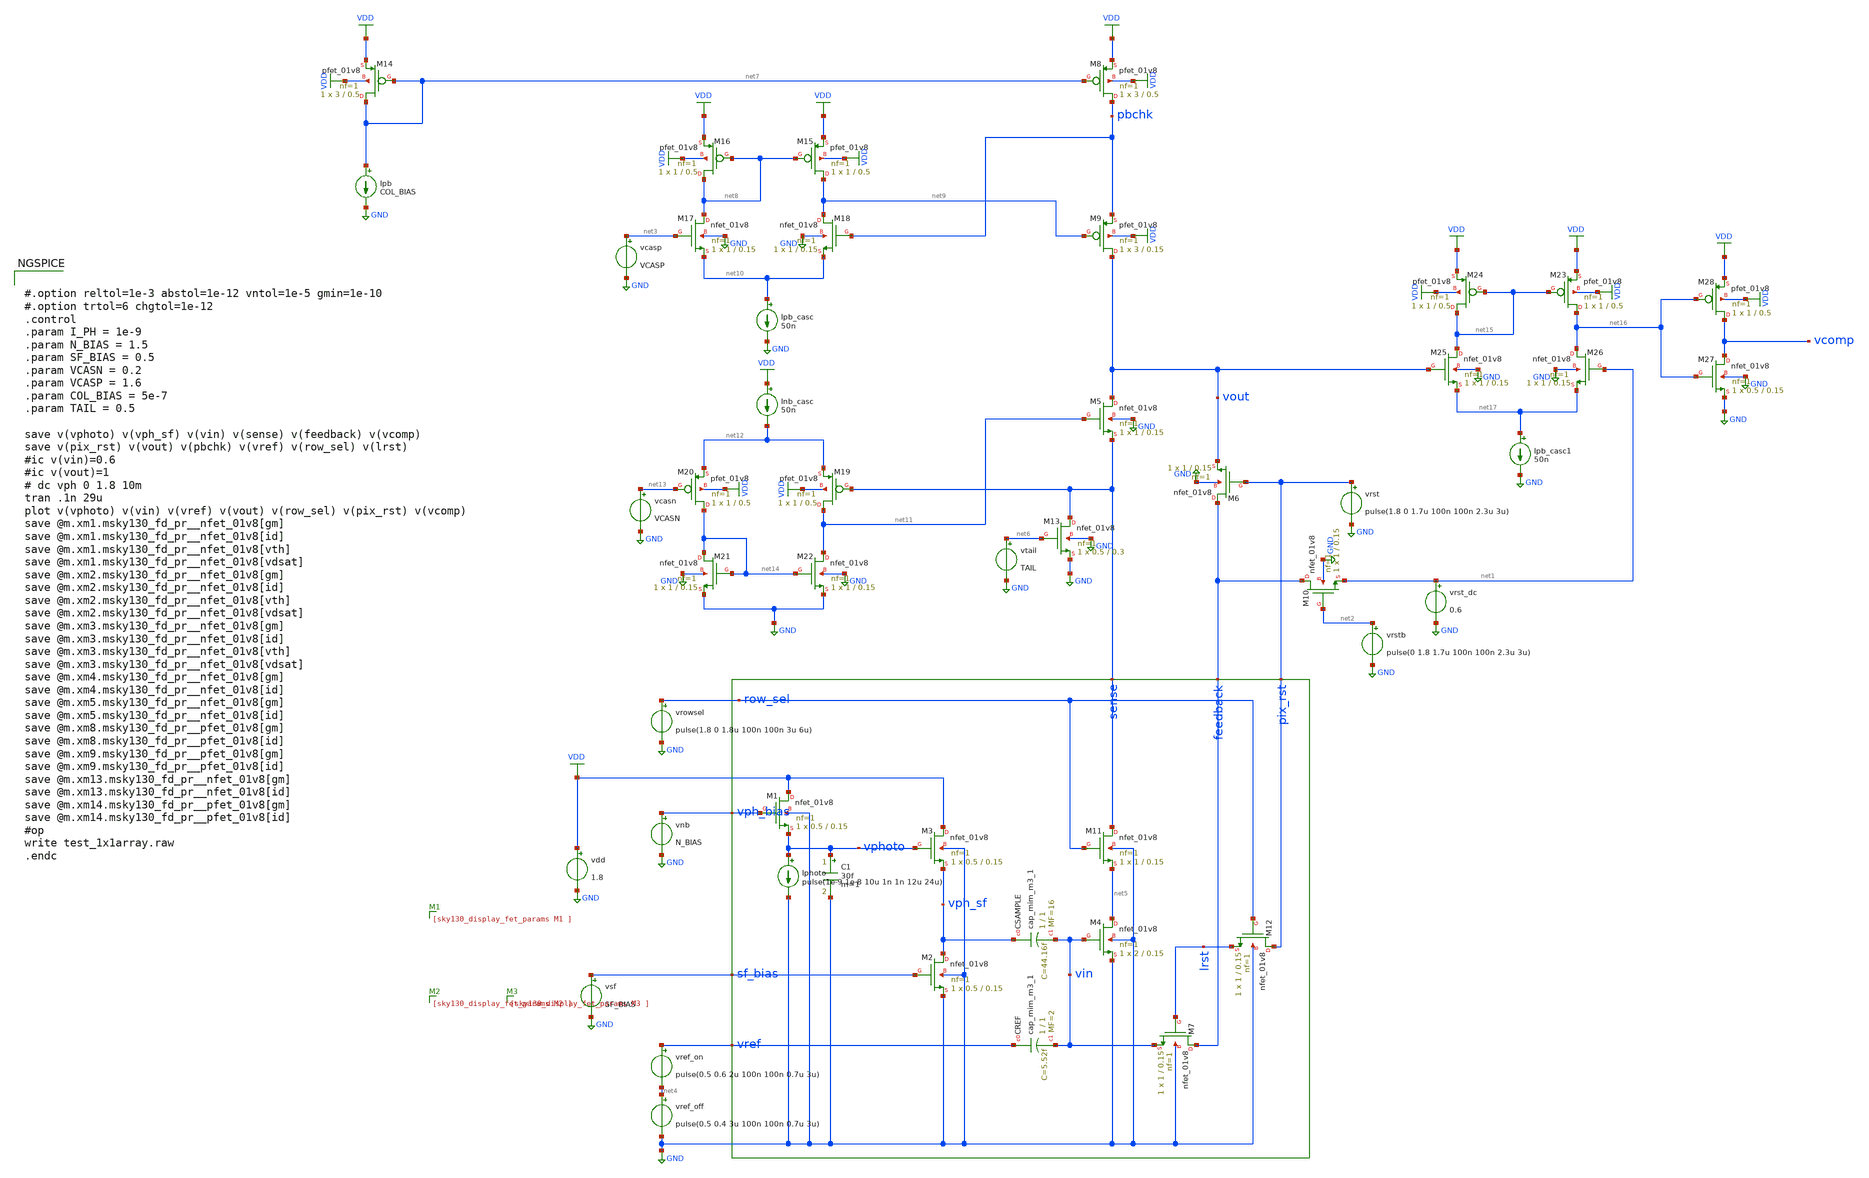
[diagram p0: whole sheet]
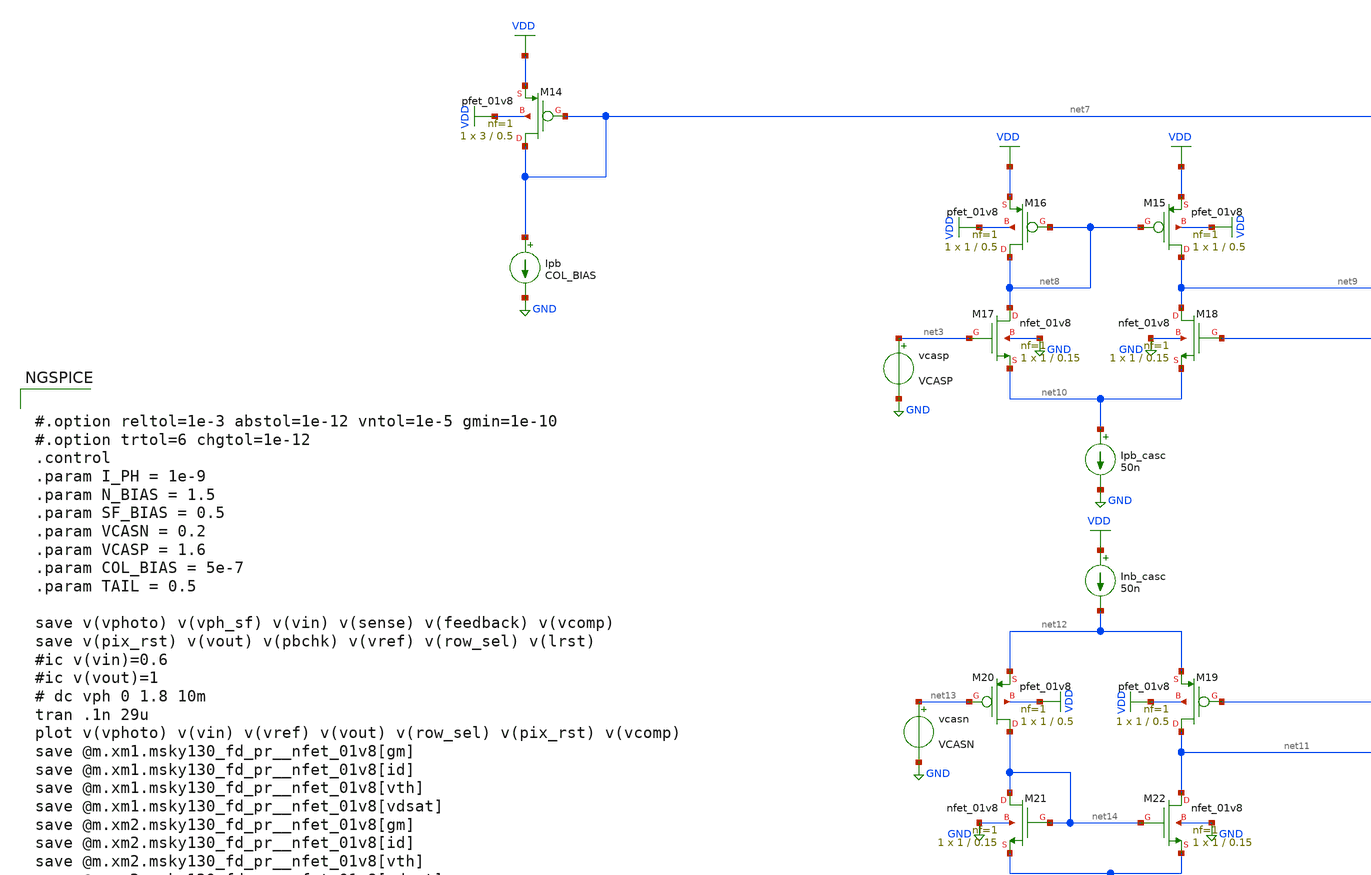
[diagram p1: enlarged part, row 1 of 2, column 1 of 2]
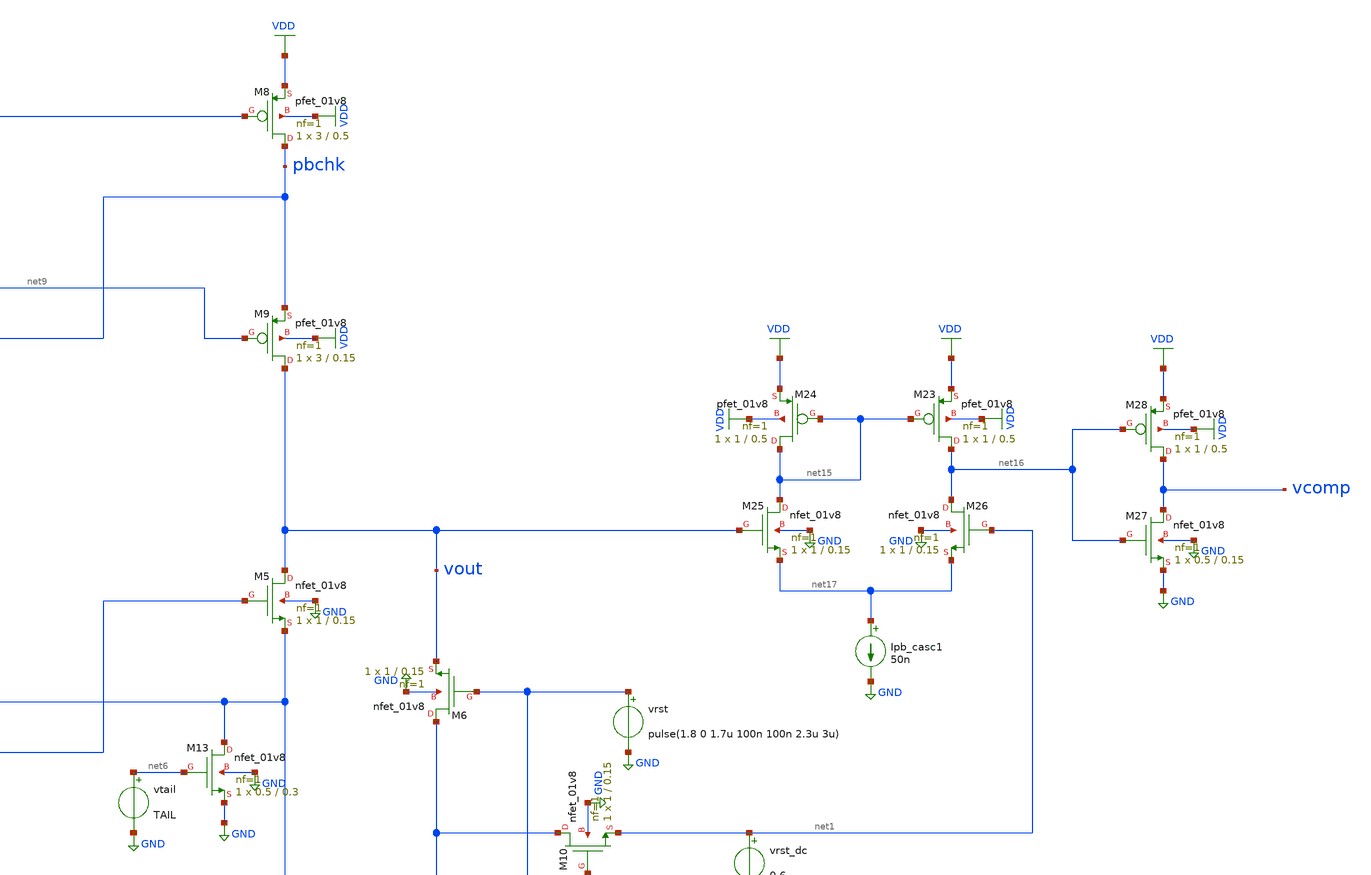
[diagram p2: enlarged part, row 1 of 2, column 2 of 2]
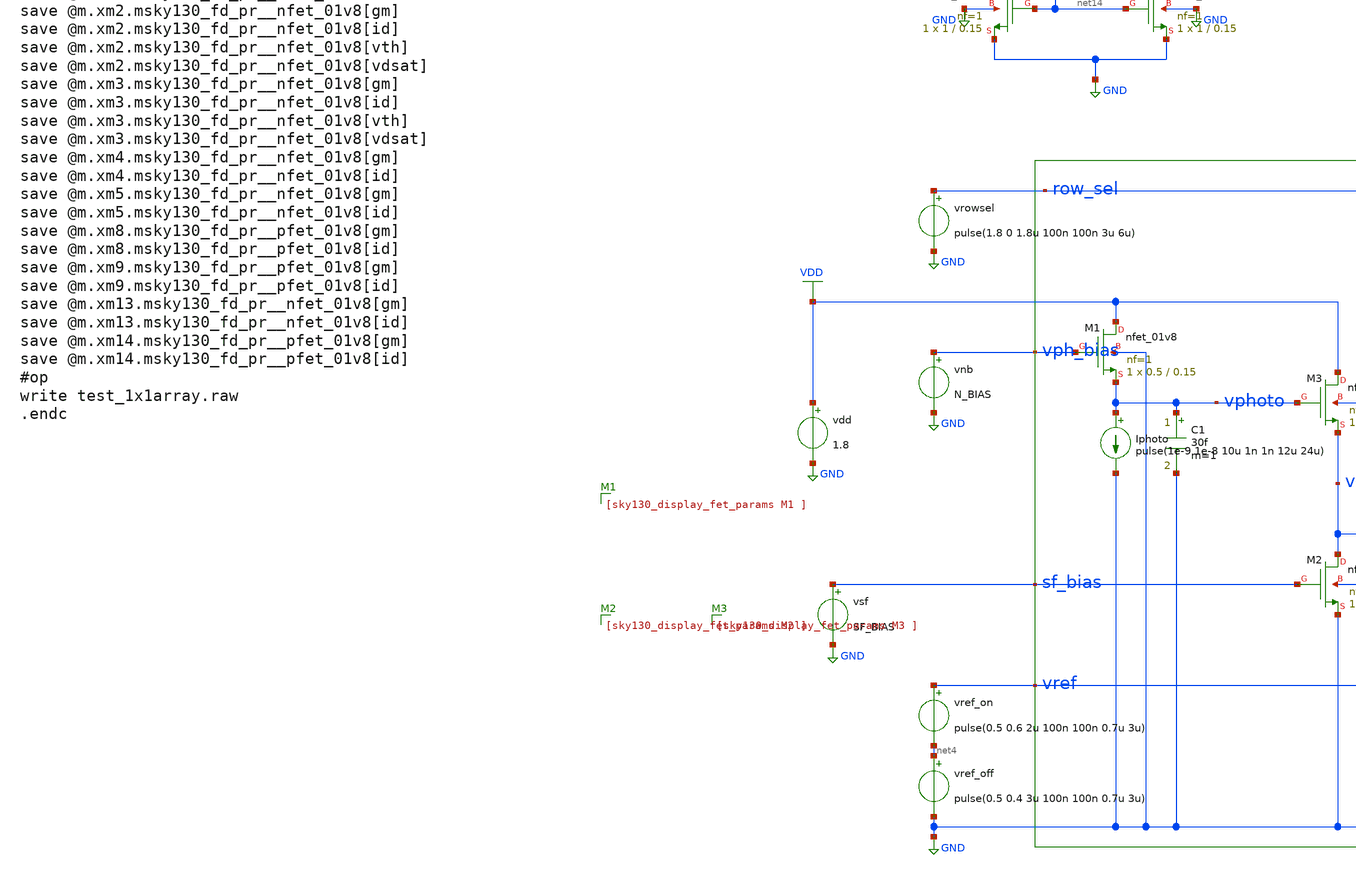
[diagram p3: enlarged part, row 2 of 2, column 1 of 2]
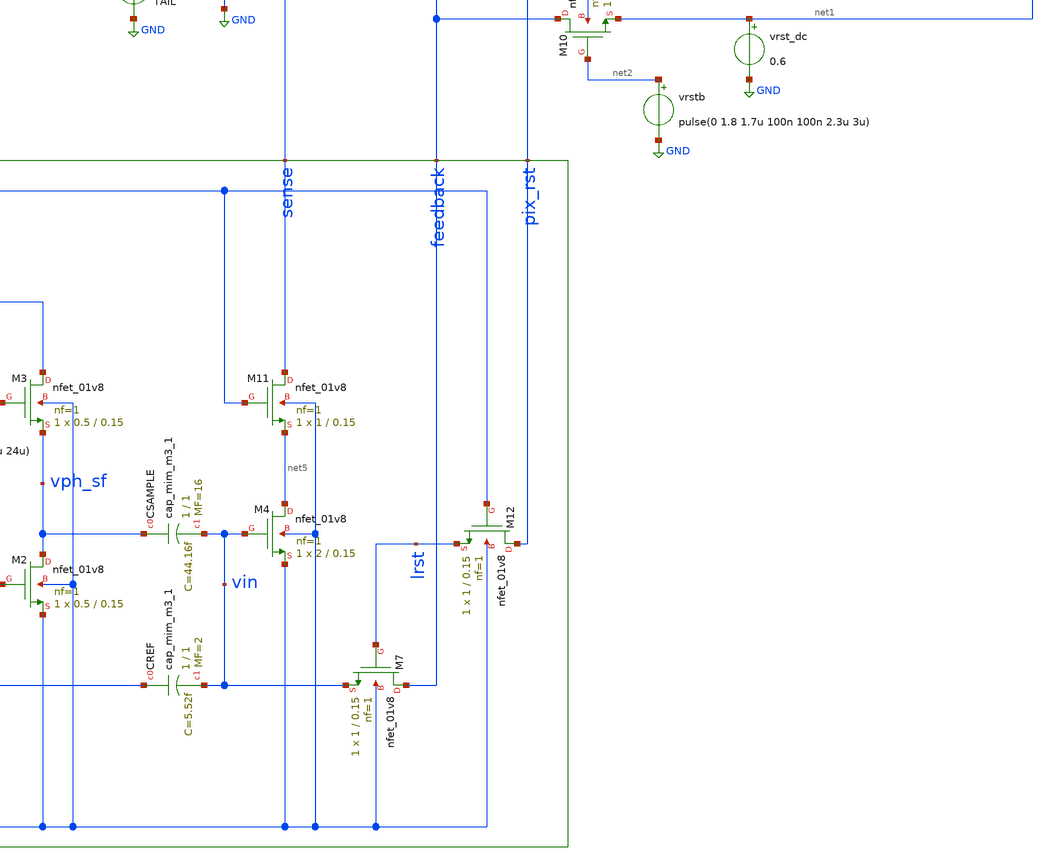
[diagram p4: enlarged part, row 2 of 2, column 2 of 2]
** sch_path: analog/xschem/test_1x1array_v1_good.sch
**.subckt test_1x1array_v1_good
vdd VDD GND 1.8
.save i(vdd)
XCSAMPLE vph_sf vin sky130_fd_pr__cap_mim_m3_1 W=1 L=1 MF=16 m=16
XCREF vref vin sky130_fd_pr__cap_mim_m3_1 W=1 L=1 MF=2 m=2
C1 vphoto GND 30f m=1
XM1 VDD vph_bias vphoto GND sky130_fd_pr__nfet_01v8 L=0.15 W=0.5 nf=1 ad='int((1 + 1)/2) * 0.5 / 1 * 0.29'
+ as='int((1 + 2)/2) * 0.5 / 1 * 0.29' pd='2*int((1 + 1)/2) * (0.5 / 1 + 0.29)' ps='2*int((1 + 2)/2) * (0.5 / 1 + 0.29)'
+ nrd='0.29 / 0.5 ' nrs='0.29 / 0.5 ' sa=0 sb=0 sd=0 mult=1 m=1
vnb vph_bias GND N_BIAS
vsf sf_bias GND SF_BIAS
vref_on vref net4 pulse(0.5 0.6 2u 100n 100n 0.7u 3u)
Iphoto vphoto GND pulse(1e-9 1e-8 10u 1n 1n 12u 24u)
XM4 net5 vin GND GND sky130_fd_pr__nfet_01v8 L=0.15 W=2 nf=1 ad='int((1 + 1)/2) * 2 / 1 * 0.29' as='int((1 + 2)/2) * 2 / 1 * 0.29'
+ pd='2*int((1 + 1)/2) * (2 / 1 + 0.29)' ps='2*int((1 + 2)/2) * (2 / 1 + 0.29)' nrd='0.29 / 2 ' nrs='0.29 / 2 '
+ sa=0 sb=0 sd=0 mult=1 m=1
XM5 vout net11 sense GND sky130_fd_pr__nfet_01v8 L=0.15 W=1 nf=1 ad='int((1 + 1)/2) * 1 / 1 * 0.29' as='int((1 + 2)/2) * 1 / 1 * 0.29'
+ pd='2*int((1 + 1)/2) * (1 / 1 + 0.29)' ps='2*int((1 + 2)/2) * (1 / 1 + 0.29)' nrd='0.29 / 1 ' nrs='0.29 / 1 '
+ sa=0 sb=0 sd=0 mult=1 m=1
vcasn net13 GND VCASN
XM6 feedback pix_rst vout GND sky130_fd_pr__nfet_01v8 L=0.15 W=1 nf=1 ad='int((1 + 1)/2) * 1 / 1 * 0.29'
+ as='int((1 + 2)/2) * 1 / 1 * 0.29' pd='2*int((1 + 1)/2) * (1 / 1 + 0.29)' ps='2*int((1 + 2)/2) * (1 / 1 + 0.29)'
+ nrd='0.29 / 1 ' nrs='0.29 / 1 ' sa=0 sb=0 sd=0 mult=1 m=1
XM7 feedback lrst vin GND sky130_fd_pr__nfet_01v8 L=0.15 W=1 nf=1 ad='int((1 + 1)/2) * 1 / 1 * 0.29'
+ as='int((1 + 2)/2) * 1 / 1 * 0.29' pd='2*int((1 + 1)/2) * (1 / 1 + 0.29)' ps='2*int((1 + 2)/2) * (1 / 1 + 0.29)'
+ nrd='0.29 / 1 ' nrs='0.29 / 1 ' sa=0 sb=0 sd=0 mult=1 m=1
vrst pix_rst GND pulse(1.8 0 1.7u 100n 100n 2.3u 3u)
Ipb net7 GND COL_BIAS
XM8 pbchk net7 VDD VDD sky130_fd_pr__pfet_01v8 L=0.5 W=3 nf=1 ad='int((1 + 1)/2) * 3 / 1 * 0.29' as='int((1 + 2)/2) * 3 / 1 * 0.29'
+ pd='2*int((1 + 1)/2) * (3 / 1 + 0.29)' ps='2*int((1 + 2)/2) * (3 / 1 + 0.29)' nrd='0.29 / 3 ' nrs='0.29 / 3 '
+ sa=0 sb=0 sd=0 mult=1 m=1
XM9 vout net9 pbchk VDD sky130_fd_pr__pfet_01v8 L=0.15 W=3 nf=1 ad='int((1 + 1)/2) * 3 / 1 * 0.29' as='int((1 + 2)/2) * 3 / 1 * 0.29'
+ pd='2*int((1 + 1)/2) * (3 / 1 + 0.29)' ps='2*int((1 + 2)/2) * (3 / 1 + 0.29)' nrd='0.29 / 3 ' nrs='0.29 / 3 '
+ sa=0 sb=0 sd=0 mult=1 m=1
vcasp net3 GND VCASP
XM10 feedback net2 net1 GND sky130_fd_pr__nfet_01v8 L=0.15 W=1 nf=1 ad='int((1 + 1)/2) * 1 / 1 * 0.29'
+ as='int((1 + 2)/2) * 1 / 1 * 0.29' pd='2*int((1 + 1)/2) * (1 / 1 + 0.29)' ps='2*int((1 + 2)/2) * (1 / 1 + 0.29)'
+ nrd='0.29 / 1 ' nrs='0.29 / 1 ' sa=0 sb=0 sd=0 mult=1 m=1
vrstb net2 GND pulse(0 1.8 1.7u 100n 100n 2.3u 3u)
vrst_dc net1 GND 0.6
vref_off net4 GND pulse(0.5 0.4 3u 100n 100n 0.7u 3u)
XM2 vph_sf sf_bias GND GND sky130_fd_pr__nfet_01v8 L=0.15 W=0.5 nf=1 ad='int((1 + 1)/2) * 0.5 / 1 * 0.29'
+ as='int((1 + 2)/2) * 0.5 / 1 * 0.29' pd='2*int((1 + 1)/2) * (0.5 / 1 + 0.29)' ps='2*int((1 + 2)/2) * (0.5 / 1 + 0.29)'
+ nrd='0.29 / 0.5 ' nrs='0.29 / 0.5 ' sa=0 sb=0 sd=0 mult=1 m=1
XM3 VDD vphoto vph_sf GND sky130_fd_pr__nfet_01v8 L=0.15 W=0.5 nf=1 ad='int((1 + 1)/2) * 0.5 / 1 * 0.29'
+ as='int((1 + 2)/2) * 0.5 / 1 * 0.29' pd='2*int((1 + 1)/2) * (0.5 / 1 + 0.29)' ps='2*int((1 + 2)/2) * (0.5 / 1 + 0.29)'
+ nrd='0.29 / 0.5 ' nrs='0.29 / 0.5 ' sa=0 sb=0 sd=0 mult=1 m=1
XM11 sense row_sel net5 GND sky130_fd_pr__nfet_01v8 L=0.15 W=1 nf=1 ad='int((1 + 1)/2) * 1 / 1 * 0.29'
+ as='int((1 + 2)/2) * 1 / 1 * 0.29' pd='2*int((1 + 1)/2) * (1 / 1 + 0.29)' ps='2*int((1 + 2)/2) * (1 / 1 + 0.29)'
+ nrd='0.29 / 1 ' nrs='0.29 / 1 ' sa=0 sb=0 sd=0 mult=1 m=1
XM12 pix_rst row_sel lrst GND sky130_fd_pr__nfet_01v8 L=0.15 W=1 nf=1 ad='int((1 + 1)/2) * 1 / 1 * 0.29'
+ as='int((1 + 2)/2) * 1 / 1 * 0.29' pd='2*int((1 + 1)/2) * (1 / 1 + 0.29)' ps='2*int((1 + 2)/2) * (1 / 1 + 0.29)'
+ nrd='0.29 / 1 ' nrs='0.29 / 1 ' sa=0 sb=0 sd=0 mult=1 m=1
vrowsel row_sel GND pulse(1.8 0 1.8u 100n 100n 3u 6u)
vtail net6 GND TAIL
XM13 sense net6 GND GND sky130_fd_pr__nfet_01v8 L=0.3 W=0.5 nf=1 ad='int((1 + 1)/2) * 0.5 / 1 * 0.29'
+ as='int((1 + 2)/2) * 0.5 / 1 * 0.29' pd='2*int((1 + 1)/2) * (0.5 / 1 + 0.29)' ps='2*int((1 + 2)/2) * (0.5 / 1 + 0.29)'
+ nrd='0.29 / 0.5 ' nrs='0.29 / 0.5 ' sa=0 sb=0 sd=0 mult=1 m=1
XM14 net7 net7 VDD VDD sky130_fd_pr__pfet_01v8 L=0.5 W=3 nf=1 ad='int((1 + 1)/2) * 3 / 1 * 0.29' as='int((1 + 2)/2) * 3 / 1 * 0.29'
+ pd='2*int((1 + 1)/2) * (3 / 1 + 0.29)' ps='2*int((1 + 2)/2) * (3 / 1 + 0.29)' nrd='0.29 / 3 ' nrs='0.29 / 3 '
+ sa=0 sb=0 sd=0 mult=1 m=1
XM15 net9 net8 VDD VDD sky130_fd_pr__pfet_01v8 L=0.5 W=1 nf=1 ad='int((1 + 1)/2) * 1 / 1 * 0.29' as='int((1 + 2)/2) * 1 / 1 * 0.29'
+ pd='2*int((1 + 1)/2) * (1 / 1 + 0.29)' ps='2*int((1 + 2)/2) * (1 / 1 + 0.29)' nrd='0.29 / 1 ' nrs='0.29 / 1 '
+ sa=0 sb=0 sd=0 mult=1 m=1
XM16 net8 net8 VDD VDD sky130_fd_pr__pfet_01v8 L=0.5 W=1 nf=1 ad='int((1 + 1)/2) * 1 / 1 * 0.29' as='int((1 + 2)/2) * 1 / 1 * 0.29'
+ pd='2*int((1 + 1)/2) * (1 / 1 + 0.29)' ps='2*int((1 + 2)/2) * (1 / 1 + 0.29)' nrd='0.29 / 1 ' nrs='0.29 / 1 '
+ sa=0 sb=0 sd=0 mult=1 m=1
XM17 net8 net3 net10 GND sky130_fd_pr__nfet_01v8 L=0.15 W=1 nf=1 ad='int((1 + 1)/2) * 1 / 1 * 0.29' as='int((1 + 2)/2) * 1 / 1 * 0.29'
+ pd='2*int((1 + 1)/2) * (1 / 1 + 0.29)' ps='2*int((1 + 2)/2) * (1 / 1 + 0.29)' nrd='0.29 / 1 ' nrs='0.29 / 1 '
+ sa=0 sb=0 sd=0 mult=1 m=1
XM18 net9 pbchk net10 GND sky130_fd_pr__nfet_01v8 L=0.15 W=1 nf=1 ad='int((1 + 1)/2) * 1 / 1 * 0.29'
+ as='int((1 + 2)/2) * 1 / 1 * 0.29' pd='2*int((1 + 1)/2) * (1 / 1 + 0.29)' ps='2*int((1 + 2)/2) * (1 / 1 + 0.29)'
+ nrd='0.29 / 1 ' nrs='0.29 / 1 ' sa=0 sb=0 sd=0 mult=1 m=1
Ipb_casc net10 GND 50n
XM19 net11 sense net12 VDD sky130_fd_pr__pfet_01v8 L=0.5 W=1 nf=1 ad='int((1 + 1)/2) * 1 / 1 * 0.29'
+ as='int((1 + 2)/2) * 1 / 1 * 0.29' pd='2*int((1 + 1)/2) * (1 / 1 + 0.29)' ps='2*int((1 + 2)/2) * (1 / 1 + 0.29)'
+ nrd='0.29 / 1 ' nrs='0.29 / 1 ' sa=0 sb=0 sd=0 mult=1 m=1
Inb_casc VDD net12 50n
XM20 net14 net13 net12 VDD sky130_fd_pr__pfet_01v8 L=0.5 W=1 nf=1 ad='int((1 + 1)/2) * 1 / 1 * 0.29'
+ as='int((1 + 2)/2) * 1 / 1 * 0.29' pd='2*int((1 + 1)/2) * (1 / 1 + 0.29)' ps='2*int((1 + 2)/2) * (1 / 1 + 0.29)'
+ nrd='0.29 / 1 ' nrs='0.29 / 1 ' sa=0 sb=0 sd=0 mult=1 m=1
XM21 net14 net14 GND GND sky130_fd_pr__nfet_01v8 L=0.15 W=1 nf=1 ad='int((1 + 1)/2) * 1 / 1 * 0.29' as='int((1 + 2)/2) * 1 / 1 * 0.29'
+ pd='2*int((1 + 1)/2) * (1 / 1 + 0.29)' ps='2*int((1 + 2)/2) * (1 / 1 + 0.29)' nrd='0.29 / 1 ' nrs='0.29 / 1 '
+ sa=0 sb=0 sd=0 mult=1 m=1
XM22 net11 net14 GND GND sky130_fd_pr__nfet_01v8 L=0.15 W=1 nf=1 ad='int((1 + 1)/2) * 1 / 1 * 0.29' as='int((1 + 2)/2) * 1 / 1 * 0.29'
+ pd='2*int((1 + 1)/2) * (1 / 1 + 0.29)' ps='2*int((1 + 2)/2) * (1 / 1 + 0.29)' nrd='0.29 / 1 ' nrs='0.29 / 1 '
+ sa=0 sb=0 sd=0 mult=1 m=1
XM23 net16 net15 VDD VDD sky130_fd_pr__pfet_01v8 L=0.5 W=1 nf=1 ad='int((1 + 1)/2) * 1 / 1 * 0.29' as='int((1 + 2)/2) * 1 / 1 * 0.29'
+ pd='2*int((1 + 1)/2) * (1 / 1 + 0.29)' ps='2*int((1 + 2)/2) * (1 / 1 + 0.29)' nrd='0.29 / 1 ' nrs='0.29 / 1 '
+ sa=0 sb=0 sd=0 mult=1 m=1
XM24 net15 net15 VDD VDD sky130_fd_pr__pfet_01v8 L=0.5 W=1 nf=1 ad='int((1 + 1)/2) * 1 / 1 * 0.29' as='int((1 + 2)/2) * 1 / 1 * 0.29'
+ pd='2*int((1 + 1)/2) * (1 / 1 + 0.29)' ps='2*int((1 + 2)/2) * (1 / 1 + 0.29)' nrd='0.29 / 1 ' nrs='0.29 / 1 '
+ sa=0 sb=0 sd=0 mult=1 m=1
XM25 net15 vout net17 GND sky130_fd_pr__nfet_01v8 L=0.15 W=1 nf=1 ad='int((1 + 1)/2) * 1 / 1 * 0.29'
+ as='int((1 + 2)/2) * 1 / 1 * 0.29' pd='2*int((1 + 1)/2) * (1 / 1 + 0.29)' ps='2*int((1 + 2)/2) * (1 / 1 + 0.29)'
+ nrd='0.29 / 1 ' nrs='0.29 / 1 ' sa=0 sb=0 sd=0 mult=1 m=1
XM26 net16 net1 net17 GND sky130_fd_pr__nfet_01v8 L=0.15 W=1 nf=1 ad='int((1 + 1)/2) * 1 / 1 * 0.29'
+ as='int((1 + 2)/2) * 1 / 1 * 0.29' pd='2*int((1 + 1)/2) * (1 / 1 + 0.29)' ps='2*int((1 + 2)/2) * (1 / 1 + 0.29)'
+ nrd='0.29 / 1 ' nrs='0.29 / 1 ' sa=0 sb=0 sd=0 mult=1 m=1
Ipb_casc1 net17 GND 50n
XM27 vcomp net16 GND GND sky130_fd_pr__nfet_01v8 L=0.15 W=0.5 nf=1 ad='int((1 + 1)/2) * 0.5 / 1 * 0.29'
+ as='int((1 + 2)/2) * 0.5 / 1 * 0.29' pd='2*int((1 + 1)/2) * (0.5 / 1 + 0.29)' ps='2*int((1 + 2)/2) * (0.5 / 1 + 0.29)'
+ nrd='0.29 / 0.5 ' nrs='0.29 / 0.5 ' sa=0 sb=0 sd=0 mult=1 m=1
XM28 vcomp net16 VDD VDD sky130_fd_pr__pfet_01v8 L=0.5 W=1 nf=1 ad='int((1 + 1)/2) * 1 / 1 * 0.29' as='int((1 + 2)/2) * 1 / 1 * 0.29'
+ pd='2*int((1 + 1)/2) * (1 / 1 + 0.29)' ps='2*int((1 + 2)/2) * (1 / 1 + 0.29)' nrd='0.29 / 1 ' nrs='0.29 / 1 '
+ sa=0 sb=0 sd=0 mult=1 m=1
**** begin user architecture code

** opencircuitdesign pdks install
.lib $::SKYWATER_MODELS/sky130.lib.spice tt



#.option reltol=1e-3 abstol=1e-12 vntol=1e-5 gmin=1e-10
#.option trtol=6 chgtol=1e-12
.control
.param I_PH = 1e-9
.param N_BIAS = 1.5
.param SF_BIAS = 0.5
.param VCASN = 0.2
.param VCASP = 1.6
.param COL_BIAS = 5e-7
.param TAIL = 0.5

save v(vphoto) v(vph_sf) v(vin) v(sense) v(feedback) v(vcomp)
save v(pix_rst) v(vout) v(pbchk) v(vref) v(row_sel) v(lrst)
#ic v(vin)=0.6
#ic v(vout)=1
# dc vph 0 1.8 10m
tran .1n 29u
plot v(vphoto) v(vin) v(vref) v(vout) v(row_sel) v(pix_rst) v(vcomp)
save @m.xm1.msky130_fd_pr__nfet_01v8[gm]
save @m.xm1.msky130_fd_pr__nfet_01v8[id]
save @m.xm1.msky130_fd_pr__nfet_01v8[vth]
save @m.xm1.msky130_fd_pr__nfet_01v8[vdsat]
save @m.xm2.msky130_fd_pr__nfet_01v8[gm]
save @m.xm2.msky130_fd_pr__nfet_01v8[id]
save @m.xm2.msky130_fd_pr__nfet_01v8[vth]
save @m.xm2.msky130_fd_pr__nfet_01v8[vdsat]
save @m.xm3.msky130_fd_pr__nfet_01v8[gm]
save @m.xm3.msky130_fd_pr__nfet_01v8[id]
save @m.xm3.msky130_fd_pr__nfet_01v8[vth]
save @m.xm3.msky130_fd_pr__nfet_01v8[vdsat]
save @m.xm4.msky130_fd_pr__nfet_01v8[gm]
save @m.xm4.msky130_fd_pr__nfet_01v8[id]
save @m.xm5.msky130_fd_pr__nfet_01v8[gm]
save @m.xm5.msky130_fd_pr__nfet_01v8[id]
save @m.xm8.msky130_fd_pr__pfet_01v8[gm]
save @m.xm8.msky130_fd_pr__pfet_01v8[id]
save @m.xm9.msky130_fd_pr__pfet_01v8[gm]
save @m.xm9.msky130_fd_pr__pfet_01v8[id]
save @m.xm13.msky130_fd_pr__nfet_01v8[gm]
save @m.xm13.msky130_fd_pr__nfet_01v8[id]
save @m.xm14.msky130_fd_pr__pfet_01v8[gm]
save @m.xm14.msky130_fd_pr__pfet_01v8[id]
#op
write test_1x1array.raw
.endc


**** end user architecture code
**.ends
.GLOBAL VDD
.GLOBAL GND
.end
